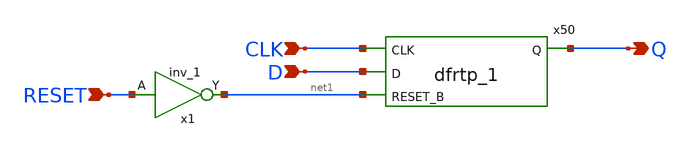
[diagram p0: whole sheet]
** sch_path: my_df.sch
**.subckt my_df CLK D RESET Q
*.ipin CLK
*.ipin D
*.ipin RESET
*.opin Q
x50 CLK D net1 GND GND VDD VDD Q sky130_fd_sc_hd__dfrtp_1
x1 RESET GND GND VDD VDD net1 sky130_fd_sc_hd__inv_1
**.ends
.end
